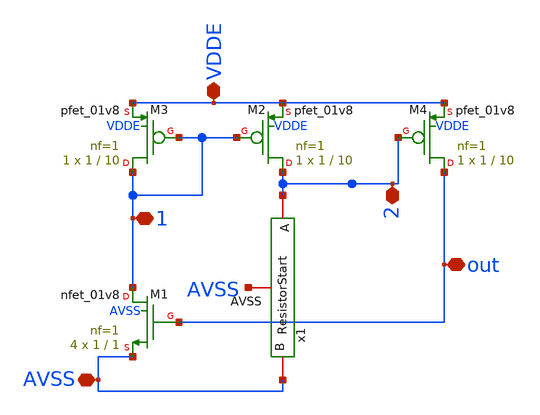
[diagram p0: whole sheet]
** sch_path: xschem/Startup.sch
**.subckt Startup VDDE AVSS out 1 2
*.iopin VDDE
*.iopin AVSS
*.iopin out
*.iopin 1
*.iopin 2
XM1 1 out AVSS AVSS sky130_fd_pr__nfet_01v8 L=1 W=1 nf=1 ad='int((nf+1)/2) * W/nf * 0.29' as='int((nf+2)/2) * W/nf * 0.29'
+ pd='2*int((nf+1)/2) * (W/nf + 0.29)' ps='2*int((nf+2)/2) * (W/nf + 0.29)' nrd='0.29 / W' nrs='0.29 / W'
+ sa=0 sb=0 sd=0 mult=4 m=4
XM2 2 1 VDDE VDDE sky130_fd_pr__pfet_01v8 L=10 W=1 nf=1 ad='int((nf+1)/2) * W/nf * 0.29' as='int((nf+2)/2) * W/nf * 0.29'
+ pd='2*int((nf+1)/2) * (W/nf + 0.29)' ps='2*int((nf+2)/2) * (W/nf + 0.29)' nrd='0.29 / W' nrs='0.29 / W'
+ sa=0 sb=0 sd=0 mult=1 m=1
XM3 1 1 VDDE VDDE sky130_fd_pr__pfet_01v8 L=10 W=1 nf=1 ad='int((nf+1)/2) * W/nf * 0.29' as='int((nf+2)/2) * W/nf * 0.29'
+ pd='2*int((nf+1)/2) * (W/nf + 0.29)' ps='2*int((nf+2)/2) * (W/nf + 0.29)' nrd='0.29 / W' nrs='0.29 / W'
+ sa=0 sb=0 sd=0 mult=1 m=1
XM4 out 2 VDDE VDDE sky130_fd_pr__pfet_01v8 L=10 W=1 nf=1 ad='int((nf+1)/2) * W/nf * 0.29' as='int((nf+2)/2) * W/nf * 0.29'
+ pd='2*int((nf+1)/2) * (W/nf + 0.29)' ps='2*int((nf+2)/2) * (W/nf + 0.29)' nrd='0.29 / W' nrs='0.29 / W'
+ sa=0 sb=0 sd=0 mult=1 m=1
x1 AVSS AVSS 2 ResistorStart
**.ends

* expanding   symbol:  ResistorStart.sym # of pins=3
** sym_path: xschem/ResistorStart.sym
** sch_path: xschem/ResistorStart.sch
.subckt ResistorStart AVSS B A
*.iopin A
*.iopin B
*.iopin AVSS
XR1 net1 A AVSS sky130_fd_pr__res_high_po_0p35 L=17 mult=1 m=1
XR2 net2 net1 AVSS sky130_fd_pr__res_high_po_0p35 L={L} mult=1 m=1
XR3 net4 net2 AVSS sky130_fd_pr__res_high_po_0p35 L={L} mult=1 m=1
XR4 net3 net4 AVSS sky130_fd_pr__res_high_po_0p35 L={L} mult=1 m=1
XR5 net5 net3 AVSS sky130_fd_pr__res_high_po_0p35 L={L} mult=1 m=1
**** begin user architecture code


.param L=17


**** end user architecture code
XR6 net6 net7 AVSS sky130_fd_pr__res_high_po_0p35 L={L} mult=1 m=1
XR7 net8 net6 AVSS sky130_fd_pr__res_high_po_0p35 L={L} mult=1 m=1
XR8 net10 net8 AVSS sky130_fd_pr__res_high_po_0p35 L={L} mult=1 m=1
XR9 net9 net10 AVSS sky130_fd_pr__res_high_po_0p35 L={L} mult=1 m=1
XR10 net5 net9 AVSS sky130_fd_pr__res_high_po_0p35 L={L} mult=1 m=1
XR11 net11 net7 AVSS sky130_fd_pr__res_high_po_0p35 L={L} mult=1 m=1
XR12 net12 net11 AVSS sky130_fd_pr__res_high_po_0p35 L={L} mult=1 m=1
XR13 net14 net12 AVSS sky130_fd_pr__res_high_po_0p35 L={L} mult=1 m=1
XR14 net13 net14 AVSS sky130_fd_pr__res_high_po_0p35 L={L} mult=1 m=1
XR15 net15 net13 AVSS sky130_fd_pr__res_high_po_0p35 L={L} mult=1 m=1
XR16 net16 net17 AVSS sky130_fd_pr__res_high_po_0p35 L={L} mult=1 m=1
XR17 net18 net16 AVSS sky130_fd_pr__res_high_po_0p35 L={L} mult=1 m=1
XR18 net20 net18 AVSS sky130_fd_pr__res_high_po_0p35 L={L} mult=1 m=1
XR19 net19 net20 AVSS sky130_fd_pr__res_high_po_0p35 L={L} mult=1 m=1
XR20 net15 net19 AVSS sky130_fd_pr__res_high_po_0p35 L={L} mult=1 m=1
XR21 net21 net17 AVSS sky130_fd_pr__res_high_po_0p35 L={L} mult=1 m=1
XR22 net22 net21 AVSS sky130_fd_pr__res_high_po_0p35 L={L} mult=1 m=1
XR23 net23 net22 AVSS sky130_fd_pr__res_high_po_0p35 L={L} mult=1 m=1
XR24 net24 net23 AVSS sky130_fd_pr__res_high_po_0p35 L={L} mult=1 m=1
XR25 net25 net24 AVSS sky130_fd_pr__res_high_po_0p35 L={L} mult=1 m=1
XR26 net26 B AVSS sky130_fd_pr__res_high_po_0p35 L={L} mult=1 m=1
XR27 net27 net26 AVSS sky130_fd_pr__res_high_po_0p35 L={L} mult=1 m=1
XR28 net28 net27 AVSS sky130_fd_pr__res_high_po_0p35 L={L} mult=1 m=1
XR29 net29 net28 AVSS sky130_fd_pr__res_high_po_0p35 L={L} mult=1 m=1
XR30 net25 net29 AVSS sky130_fd_pr__res_high_po_0p35 L={L} mult=1 m=1
.ends

.end
